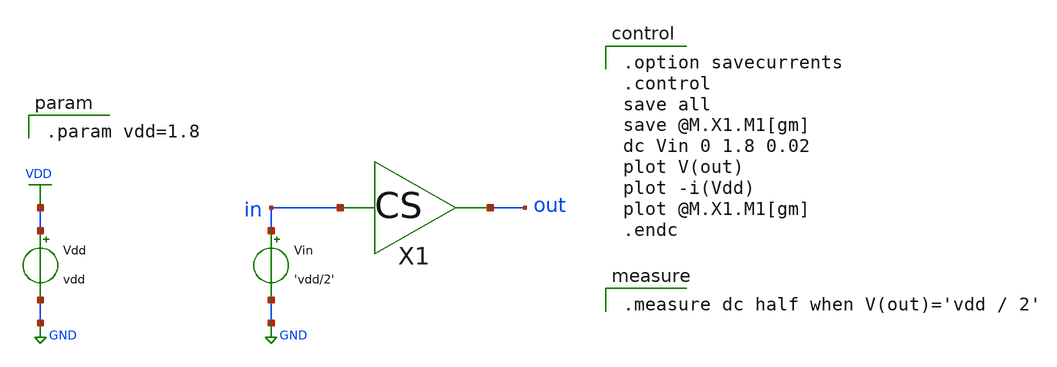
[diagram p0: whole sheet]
** sch_path: xschem/tb/dc_03_subckt.sch
**.subckt dc_03_subckt
Vdd VDD GND vdd
Vin in GND 'vdd/2'
X1 in out cs
**** begin user architecture code

.model nch nmos ( version=4.7 level=54 lmin=0.1u lmax=20u wmin=0.1u wmax=10u  )
.model pch pmos ( version=4.7 level=54 lmin=0.1u lmax=20u wmin=0.1u wmax=10u  )


.option savecurrents
.control
save all
save @M.X1.M1[gm]
dc Vin 0 1.8 0.02
plot V(out)
plot -i(Vdd)
plot @M.X1.M1[gm]
.endc


.measure dc half when V(out)='vdd / 2'


.param vdd=1.8

**** end user architecture code
**.ends

* expanding   symbol:  cs.sym # of pins=2
** sym_path: xschem/tb/cs.sym
** sch_path: xschem/tb/cs.sch
.subckt cs in out
*.ipin in
*.opin out
R1 VDD out 1k m=1
M1 out in GND GND nch w=3.6u l=0.18u m=1
.ends

.GLOBAL VDD
.GLOBAL GND
.end
